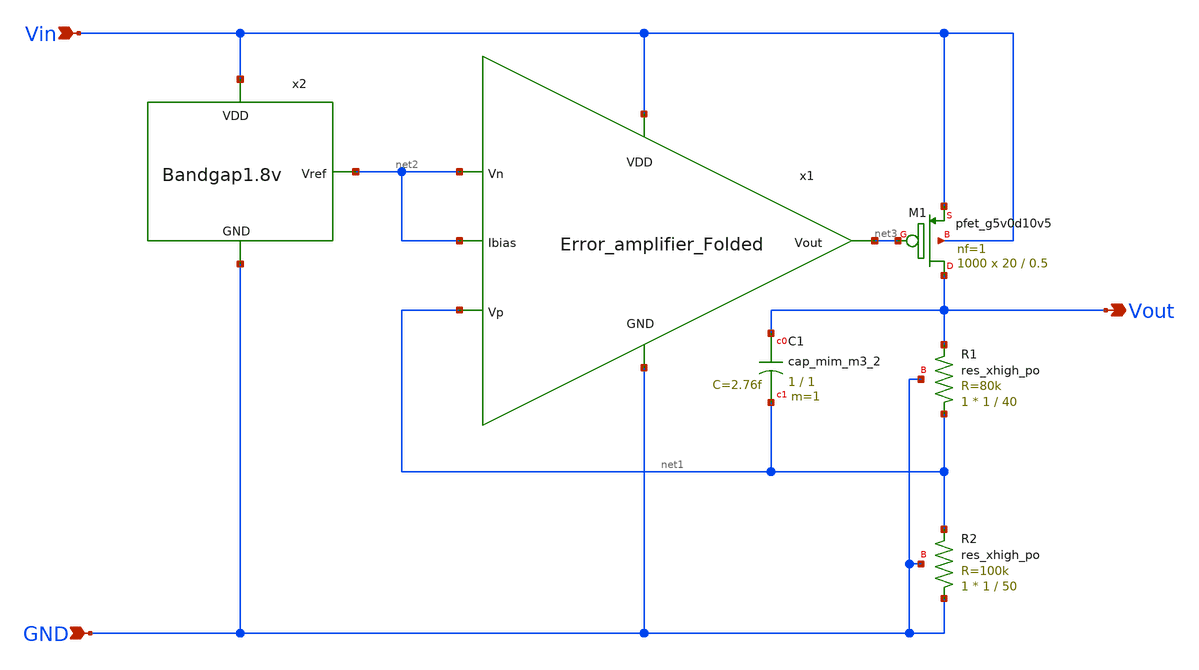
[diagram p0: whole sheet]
** sch_path: Analog_blocks/Analog_Blocks/LDO/Schematic/LDO_Folded_1.8v/LDO_Folded_1.8v.sch
**.subckt LDO_Folded_1.8v Vin GND Vout
*.ipin Vin
*.ipin GND
*.opin Vout
XR1 net1 Vout GND sky130_fd_pr__res_xhigh_po W=1 L=40 mult=1 m=1
XR2 GND net1 GND sky130_fd_pr__res_xhigh_po W=1 L=50 mult=1 m=1
XC1 Vout net1 sky130_fd_pr__cap_mim_m3_2 W=1 L=1 MF=1 m=1
XM1 Vout net3 Vin Vin sky130_fd_pr__pfet_g5v0d10v5 L=0.5 W=20 nf=1 ad='int((nf+1)/2) * W/nf * 0.29' as='int((nf+2)/2) * W/nf * 0.29'
+ pd='2*int((nf+1)/2) * (W/nf + 0.29)' ps='2*int((nf+2)/2) * (W/nf + 0.29)' nrd='0.29 / W' nrs='0.29 / W'
+ sa=0 sb=0 sd=0 mult=1000 m=1000
x1 Vin net3 net1 net2 net2 GND Error_amplifier_Folded
x2 net2 Vin GND Bandgap1.8v
**.ends
.end
